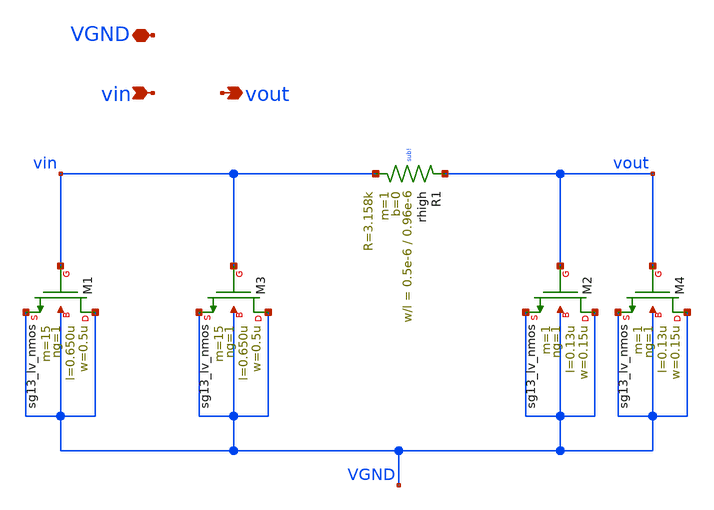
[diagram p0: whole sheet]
** sch_path: Team 2 Design/design_data/xschem/t2_loop_filter.sch
**.subckt t2_loop_filter VGND vin vout
*.iopin VGND
*.ipin vin
*.opin vout
XR1 vout vin sub! rhigh w=0.5e-6 l=0.96e-6 m=1 b=0 mm_ok=1
XM1 VGND vin VGND VGND sg13_lv_nmos w=0.5u l=0.650u ng=1 m=15 mm_ok=1
XM2 VGND vout VGND VGND sg13_lv_nmos w=0.15u l=0.13u ng=1 m=1 mm_ok=1
XM3 VGND vin VGND VGND sg13_lv_nmos w=0.5u l=0.650u ng=1 m=15 mm_ok=1
XM4 VGND vout VGND VGND sg13_lv_nmos w=0.15u l=0.13u ng=1 m=1 mm_ok=1
**.ends
.end
